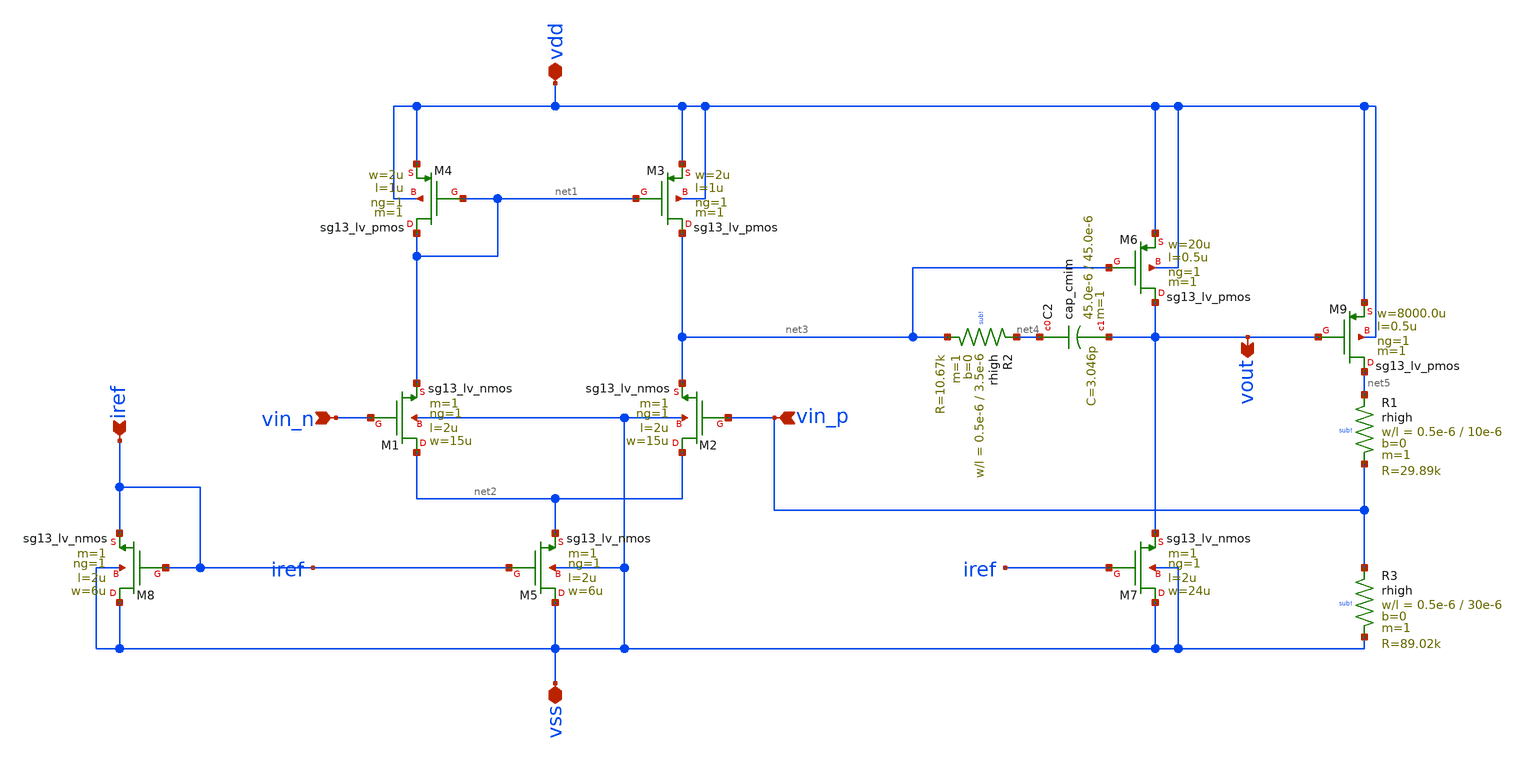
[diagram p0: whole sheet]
** sch_path: klayout/netlist/LDO.sch
**.subckt LDO iref vin_n vin_p vdd vss vout
*.ipin iref
*.ipin vin_n
*.ipin vin_p
*.iopin vdd
*.iopin vss
*.opin vout
XM1 net2 vin_n net1 vss sg13_lv_nmos w=15u l=2u ng=1 m=1 mm_ok=1
XM2 net2 vin_p net3 vss sg13_lv_nmos w=15u l=2u ng=1 m=1 mm_ok=1
XM3 net3 net1 vdd vdd sg13_lv_pmos w=2u l=1u ng=1 m=1 mm_ok=1
XM4 net1 net1 vdd vdd sg13_lv_pmos w=2u l=1u ng=1 m=1 mm_ok=1
XM5 vss iref net2 vss sg13_lv_nmos w=6u l=2u ng=1 m=1 mm_ok=1
XM8 vss iref iref vss sg13_lv_nmos w=6u l=2u ng=1 m=1 mm_ok=1
XM6 vout net3 vdd vdd sg13_lv_pmos w=20u l=0.5u ng=1 m=1 mm_ok=1
XM7 vss iref vout vss sg13_lv_nmos w=24u l=2u ng=1 m=1 mm_ok=1
XC2 net4 vout cap_cmim w=45.0e-6 l=45.0e-6 m=1 mm_ok=1
XR2 net4 net3 sub! rhigh w=0.5e-6 l=3.5e-6 m=1 b=0 mm_ok=1
XM9 net5 vout vdd vdd sg13_lv_pmos w=8000.0u l=0.5u ng=1 m=1 mm_ok=1
XR1 net5 vin_p sub! rhigh w=0.5e-6 l=10e-6 m=1 b=0 mm_ok=1
XR3 vin_p vss sub! rhigh w=0.5e-6 l=30e-6 m=1 b=0 mm_ok=1
**.ends
.end
